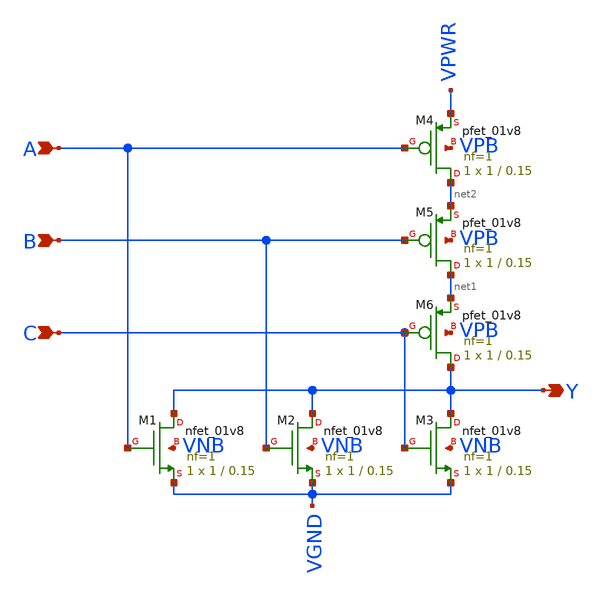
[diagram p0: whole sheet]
** sch_path: xschem/rowdec_nor3.sch
**.subckt rowdec_nor3 A Y B C
*.ipin A
*.opin Y
*.ipin B
*.ipin C
XM1 Y A VGND VNB sky130_fd_pr__nfet_01v8 L=0.15 W=1 nf=1 ad='int((nf+1)/2) * W/nf * 0.29' as='int((nf+2)/2) * W/nf * 0.29'
+ pd='2*int((nf+1)/2) * (W/nf + 0.29)' ps='2*int((nf+2)/2) * (W/nf + 0.29)' nrd='0.29 / W' nrs='0.29 / W'
+ sa=0 sb=0 sd=0 mult=1 m=1
XM2 Y B VGND VNB sky130_fd_pr__nfet_01v8 L=0.15 W=1 nf=1 ad='int((nf+1)/2) * W/nf * 0.29' as='int((nf+2)/2) * W/nf * 0.29'
+ pd='2*int((nf+1)/2) * (W/nf + 0.29)' ps='2*int((nf+2)/2) * (W/nf + 0.29)' nrd='0.29 / W' nrs='0.29 / W'
+ sa=0 sb=0 sd=0 mult=1 m=1
XM4 net2 A VPWR VPB sky130_fd_pr__pfet_01v8 L=0.15 W=1 nf=1 ad='int((nf+1)/2) * W/nf * 0.29' as='int((nf+2)/2) * W/nf * 0.29'
+ pd='2*int((nf+1)/2) * (W/nf + 0.29)' ps='2*int((nf+2)/2) * (W/nf + 0.29)' nrd='0.29 / W' nrs='0.29 / W'
+ sa=0 sb=0 sd=0 mult=1 m=1
XM3 Y C VGND VNB sky130_fd_pr__nfet_01v8 L=0.15 W=1 nf=1 ad='int((nf+1)/2) * W/nf * 0.29' as='int((nf+2)/2) * W/nf * 0.29'
+ pd='2*int((nf+1)/2) * (W/nf + 0.29)' ps='2*int((nf+2)/2) * (W/nf + 0.29)' nrd='0.29 / W' nrs='0.29 / W'
+ sa=0 sb=0 sd=0 mult=1 m=1
XM5 net1 B net2 VPB sky130_fd_pr__pfet_01v8 L=0.15 W=1 nf=1 ad='int((nf+1)/2) * W/nf * 0.29' as='int((nf+2)/2) * W/nf * 0.29'
+ pd='2*int((nf+1)/2) * (W/nf + 0.29)' ps='2*int((nf+2)/2) * (W/nf + 0.29)' nrd='0.29 / W' nrs='0.29 / W'
+ sa=0 sb=0 sd=0 mult=1 m=1
XM6 Y C net1 VPB sky130_fd_pr__pfet_01v8 L=0.15 W=1 nf=1 ad='int((nf+1)/2) * W/nf * 0.29' as='int((nf+2)/2) * W/nf * 0.29'
+ pd='2*int((nf+1)/2) * (W/nf + 0.29)' ps='2*int((nf+2)/2) * (W/nf + 0.29)' nrd='0.29 / W' nrs='0.29 / W'
+ sa=0 sb=0 sd=0 mult=1 m=1
**.ends
.end
